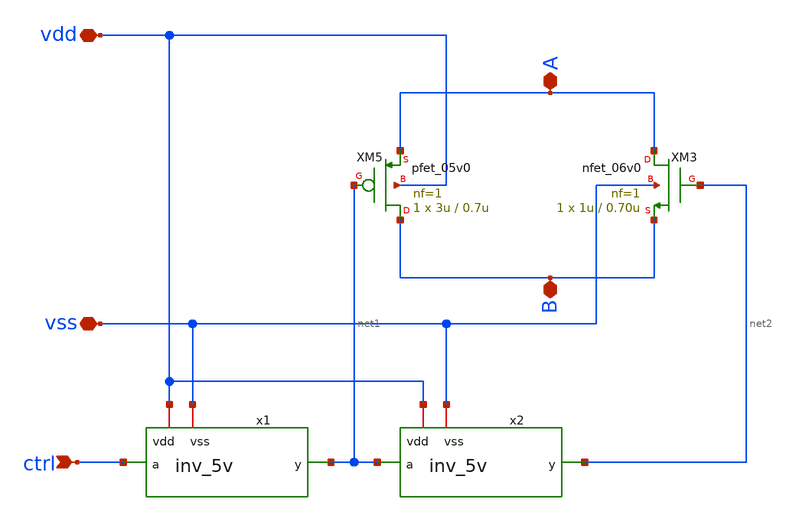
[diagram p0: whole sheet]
** sch_path: member_project/ice458/dynamic_comparator/xschem/cmos_sw_5v.sch
**.subckt cmos_sw_5v ctrl A B vdd vss
*.ipin ctrl
*.iopin A
*.iopin B
*.iopin vdd
*.iopin vss
x1 vdd ctrl net1 vss inv_5v
XM3 A net2 B vss nfet_06v0 L=0.70u W=1u nf=1 ad='int((nf+1)/2) * W/nf * 0.18u' as='int((nf+2)/2) * W/nf * 0.18u'
+ pd='2*int((nf+1)/2) * (W/nf + 0.18u)' ps='2*int((nf+2)/2) * (W/nf + 0.18u)' nrd='0.18u / W' nrs='0.18u / W'
+ sa=0 sb=0 sd=0 m=1
XM5 B net1 A vdd pfet_05v0 L=0.7u W=3u nf=1 ad='int((nf+1)/2) * W/nf * 0.18u' as='int((nf+2)/2) * W/nf * 0.18u'
+ pd='2*int((nf+1)/2) * (W/nf + 0.18u)' ps='2*int((nf+2)/2) * (W/nf + 0.18u)' nrd='0.18u / W' nrs='0.18u / W'
+ sa=0 sb=0 sd=0 m=1
x2 vdd net1 net2 vss inv_5v
**.ends

* expanding   symbol:  inv_5v.sym # of pins=4
** sym_path: member_project/ice458/dynamic_comparator/xschem/inv_5v.sym
** sch_path: member_project/ice458/dynamic_comparator/xschem/inv_5v.sch
.subckt inv_5v vdd a y vss
*.iopin vdd
*.iopin vss
*.ipin a
*.opin y
XM3 y a vss vss nfet_06v0 L=0.70u W=1u nf=1 ad='int((nf+1)/2) * W/nf * 0.18u' as='int((nf+2)/2) * W/nf * 0.18u'
+ pd='2*int((nf+1)/2) * (W/nf + 0.18u)' ps='2*int((nf+2)/2) * (W/nf + 0.18u)' nrd='0.18u / W' nrs='0.18u / W'
+ sa=0 sb=0 sd=0 m=1
XM5 y a vdd vdd pfet_05v0 L=0.7u W=3u nf=1 ad='int((nf+1)/2) * W/nf * 0.18u' as='int((nf+2)/2) * W/nf * 0.18u'
+ pd='2*int((nf+1)/2) * (W/nf + 0.18u)' ps='2*int((nf+2)/2) * (W/nf + 0.18u)' nrd='0.18u / W' nrs='0.18u / W'
+ sa=0 sb=0 sd=0 m=1
.ends

.end
